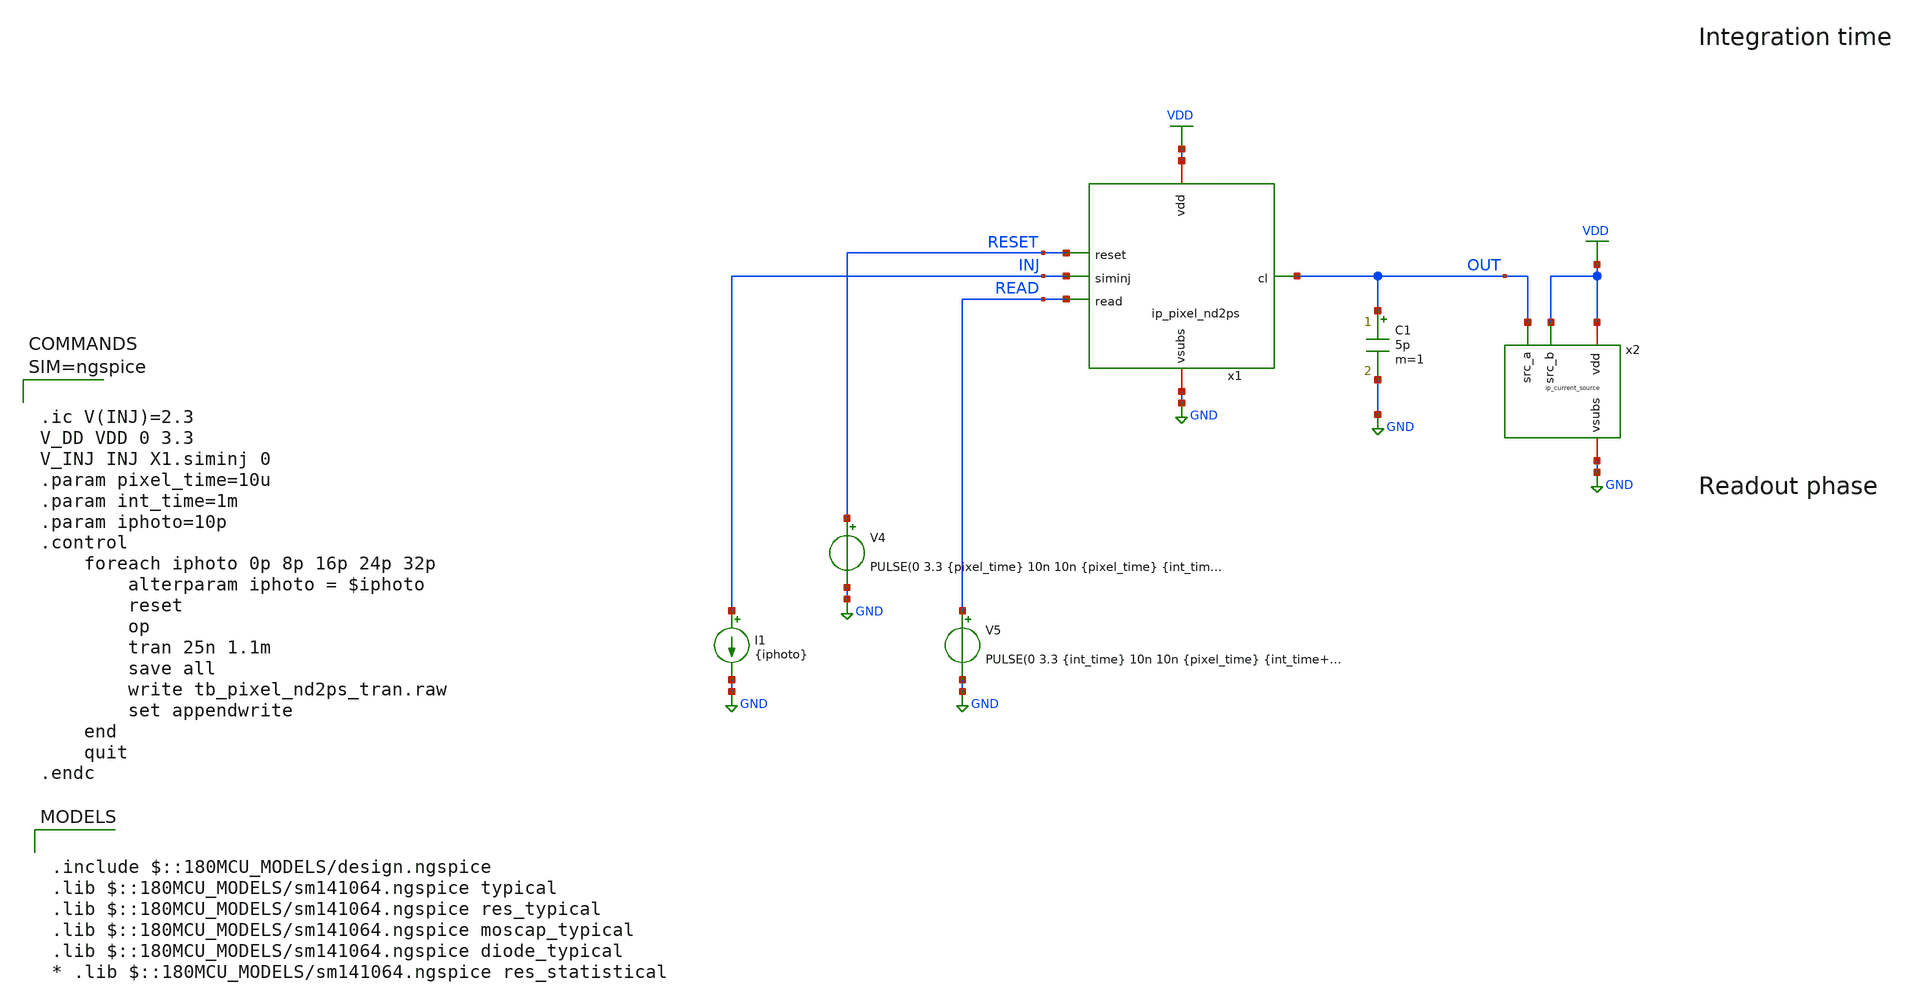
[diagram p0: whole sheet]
** sch_path: xschem/tb_pixel_nd2ps_tran.sch
**.subckt tb_pixel_nd2ps_tran
I1 INJ GND {iphoto}
V4 RESET GND PULSE(0 3.3 {pixel_time} 10n 10n {pixel_time} {int_time+10*pixel_time})
V5 READ GND PULSE(0 3.3 {int_time} 10n 10n {pixel_time} {int_time+10*pixel_time})
x2 VDD OUT GND VDD ip_current_source
x1 VDD RESET INJ READ GND OUT ip_pixel_nd2ps
C1 OUT GND 5p m=1
**** begin user architecture code

.include $::180MCU_MODELS/design.ngspice
.lib $::180MCU_MODELS/sm141064.ngspice typical
.lib $::180MCU_MODELS/sm141064.ngspice res_typical
.lib $::180MCU_MODELS/sm141064.ngspice moscap_typical
.lib $::180MCU_MODELS/sm141064.ngspice diode_typical
* .lib $::180MCU_MODELS/sm141064.ngspice res_statistical




.ic V(INJ)=2.3
V_DD VDD 0 3.3
V_INJ INJ X1.siminj 0
.param pixel_time=10u
.param int_time=1m
.param iphoto=10p
.control
	foreach iphoto 0p 8p 16p 24p 32p
		alterparam iphoto = $iphoto
		reset
		op
		tran 25n 1.1m
		save all
		write tb_pixel_nd2ps_tran.raw
		set appendwrite
	end
	quit
.endc



**** end user architecture code
**.ends

* expanding   symbol:  ip_current_source.sym # of pins=4
** sym_path: xschem/ip_current_source.sym
** sch_path: xschem/ip_current_source.sch
.subckt ip_current_source vdd src_a vsubs src_b
*.iopin vdd
*.iopin vsubs
*.ipin src_a
*.ipin src_b
XM8 refin refin vsubs vsubs nfet_06v0 L=1u W=5u nf=1 ad='int((nf+1)/2) * W/nf * 0.18u' as='int((nf+2)/2) * W/nf * 0.18u'
+ pd='2*int((nf+1)/2) * (W/nf + 0.18u)' ps='2*int((nf+2)/2) * (W/nf + 0.18u)' nrd='0.18u / W' nrs='0.18u / W'
+ sa=0 sb=0 sd=0 m=1 par=1
XM5 src_a refin net1 vsubs nfet_06v0 L=0.7u W=5u nf=1 ad='int((nf+1)/2) * W/nf * 0.18u' as='int((nf+2)/2) * W/nf * 0.18u'
+ pd='2*int((nf+1)/2) * (W/nf + 0.18u)' ps='2*int((nf+2)/2) * (W/nf + 0.18u)' nrd='0.18u / W' nrs='0.18u / W'
+ sa=0 sb=0 sd=0 m=2 par=2
XM3 src_b refin net2 vsubs nfet_06v0 L=0.7u W=5u nf=1 ad='int((nf+1)/2) * W/nf * 0.18u' as='int((nf+2)/2) * W/nf * 0.18u'
+ pd='2*int((nf+1)/2) * (W/nf + 0.18u)' ps='2*int((nf+2)/2) * (W/nf + 0.18u)' nrd='0.18u / W' nrs='0.18u / W'
+ sa=0 sb=0 sd=0 m=2 par=2
XM4 net1 refin vsubs vsubs nfet_06v0 L=5u W=0.5u nf=1 ad='int((nf+1)/2) * W/nf * 0.18u' as='int((nf+2)/2) * W/nf * 0.18u'
+ pd='2*int((nf+1)/2) * (W/nf + 0.18u)' ps='2*int((nf+2)/2) * (W/nf + 0.18u)' nrd='0.18u / W' nrs='0.18u / W'
+ sa=0 sb=0 sd=0 m=1 par=1
XM7 net2 refin vsubs vsubs nfet_06v0 L=5u W=0.5u nf=1 ad='int((nf+1)/2) * W/nf * 0.18u' as='int((nf+2)/2) * W/nf * 0.18u'
+ pd='2*int((nf+1)/2) * (W/nf + 0.18u)' ps='2*int((nf+2)/2) * (W/nf + 0.18u)' nrd='0.18u / W' nrs='0.18u / W'
+ sa=0 sb=0 sd=0 m=1 par=1
XR5 refin vdd vsubs ppolyf_u_1k_6p0 r_width=1e-6 r_length=42e-6 m=1
.ends


* expanding   symbol:  ip_pixel_nd2ps.sym # of pins=6
** sym_path: xschem/ip_pixel_nd2ps.sym
** sch_path: xschem/ip_pixel_nd2ps.sch
.subckt ip_pixel_nd2ps vdd reset siminj read vsubs cl
*.iopin vdd
*.iopin vsubs
*.ipin siminj
*.ipin reset
*.ipin read
*.opin cl
XM1 vdd reset siminj vsubs nfet_03v3 L=0.3u W=0.3u nf=1 ad='int((nf+1)/2) * W/nf * 0.18u' as='int((nf+2)/2) * W/nf * 0.18u'
+ pd='2*int((nf+1)/2) * (W/nf + 0.18u)' ps='2*int((nf+2)/2) * (W/nf + 0.18u)' nrd='0.18u / W' nrs='0.18u / W'
+ sa=0 sb=0 sd=0 m=1
XM2 vdd siminj sfout vsubs nfet_03v3 L=1u W=2.5u nf=1 ad='int((nf+1)/2) * W/nf * 0.18u' as='int((nf+2)/2) * W/nf * 0.18u'
+ pd='2*int((nf+1)/2) * (W/nf + 0.18u)' ps='2*int((nf+2)/2) * (W/nf + 0.18u)' nrd='0.18u / W' nrs='0.18u / W'
+ sa=0 sb=0 sd=0 m=1
XM3 sfout read cl vsubs nfet_03v3 L=0.3u W=0.3u nf=1 ad='int((nf+1)/2) * W/nf * 0.18u' as='int((nf+2)/2) * W/nf * 0.18u'
+ pd='2*int((nf+1)/2) * (W/nf + 0.18u)' ps='2*int((nf+2)/2) * (W/nf + 0.18u)' nrd='0.18u / W' nrs='0.18u / W'
+ sa=0 sb=0 sd=0 m=1
D1 vsubs siminj diode_nd2ps_03v3 area='13.5u * 13.5u ' pj='2*13.5u + 2*13.5u ' m=1
.ends

.GLOBAL GND
.GLOBAL VDD
.end
